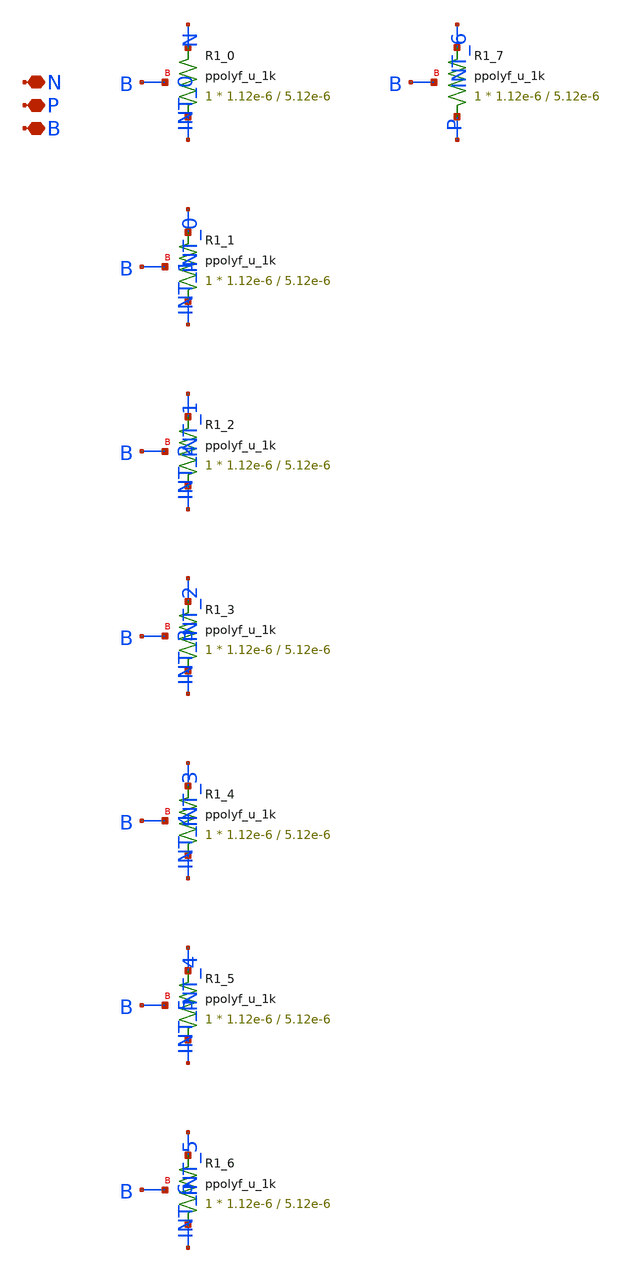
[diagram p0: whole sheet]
** sch_path: design/LELO_TR_GF180MCUD/LELOTR_RES8.sch
**.subckt LELOTR_RES8 N P B
*.iopin N
*.iopin P
*.iopin B
XR1_0 INT_0 N B ppolyf_u_1k r_width=1.12e-6 r_length=5.12e-6 m=1
XR1_1 INT_1 INT_0 B ppolyf_u_1k r_width=1.12e-6 r_length=5.12e-6 m=1
XR1_2 INT_2 INT_1 B ppolyf_u_1k r_width=1.12e-6 r_length=5.12e-6 m=1
XR1_3 INT_3 INT_2 B ppolyf_u_1k r_width=1.12e-6 r_length=5.12e-6 m=1
XR1_4 INT_4 INT_3 B ppolyf_u_1k r_width=1.12e-6 r_length=5.12e-6 m=1
XR1_5 INT_5 INT_4 B ppolyf_u_1k r_width=1.12e-6 r_length=5.12e-6 m=1
XR1_6 INT_6 INT_5 B ppolyf_u_1k r_width=1.12e-6 r_length=5.12e-6 m=1
XR1_7 P INT_6 B ppolyf_u_1k r_width=1.12e-6 r_length=5.12e-6 m=1
**.ends
.end
